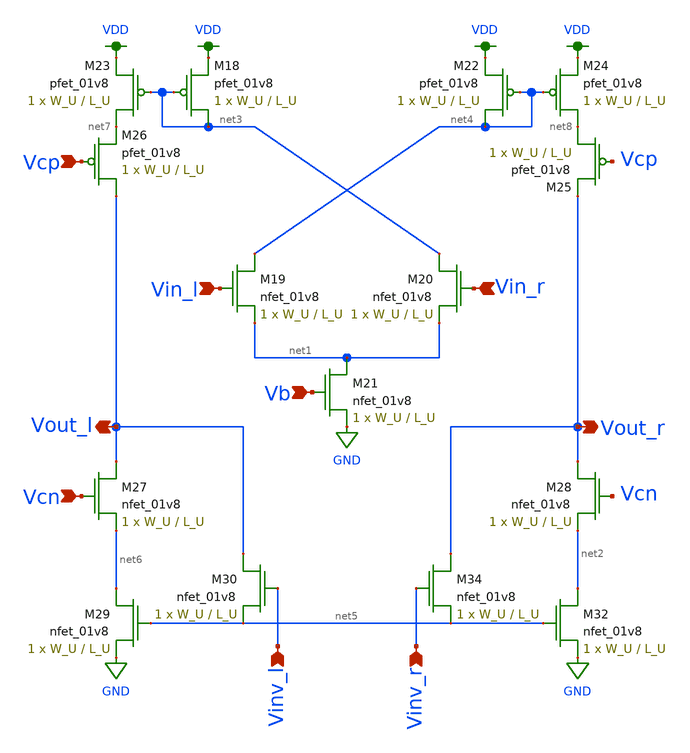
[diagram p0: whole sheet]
** sch_path: schematics/ota.sch
**.subckt ota Vin_l Vin_r Vcp Vb Vinv_l Vinv_r Vcn Vout_r Vout_l
*.ipin Vin_l
*.ipin Vin_r
*.ipin Vcp
*.ipin Vb
*.ipin Vinv_l
*.ipin Vinv_r
*.ipin Vcn
*.opin Vout_r
*.opin Vout_l
XM18 net3 net3 VDD VDD sky130_fd_pr__pfet_01v8 L=L_U W=W_U nf=1 ad='int((nf+1)/2) * W/nf * 0.29' as='int((nf+2)/2) * W/nf * 0.29'
+ pd='2*int((nf+1)/2) * (W/nf + 0.29)' ps='2*int((nf+2)/2) * (W/nf + 0.29)' nrd='0.29 / W' nrs='0.29 / W'
+ sa=0 sb=0 sd=0 mult=1 m=1
XM19 net4 Vin_l net1 GND sky130_fd_pr__nfet_01v8 L=L_U W=W_U nf=1 ad='int((nf+1)/2) * W/nf * 0.29' as='int((nf+2)/2) * W/nf * 0.29'
+ pd='2*int((nf+1)/2) * (W/nf + 0.29)' ps='2*int((nf+2)/2) * (W/nf + 0.29)' nrd='0.29 / W' nrs='0.29 / W'
+ sa=0 sb=0 sd=0 mult=1 m=1
XM20 net3 Vin_r net1 GND sky130_fd_pr__nfet_01v8 L=L_U W=W_U nf=1 ad='int((nf+1)/2) * W/nf * 0.29' as='int((nf+2)/2) * W/nf * 0.29'
+ pd='2*int((nf+1)/2) * (W/nf + 0.29)' ps='2*int((nf+2)/2) * (W/nf + 0.29)' nrd='0.29 / W' nrs='0.29 / W'
+ sa=0 sb=0 sd=0 mult=1 m=1
XM21 net1 Vb GND GND sky130_fd_pr__nfet_01v8 L=L_U W=W_U nf=1 ad='int((nf+1)/2) * W/nf * 0.29' as='int((nf+2)/2) * W/nf * 0.29'
+ pd='2*int((nf+1)/2) * (W/nf + 0.29)' ps='2*int((nf+2)/2) * (W/nf + 0.29)' nrd='0.29 / W' nrs='0.29 / W'
+ sa=0 sb=0 sd=0 mult=1 m=1
XM22 net4 net4 VDD VDD sky130_fd_pr__pfet_01v8 L=L_U W=W_U nf=1 ad='int((nf+1)/2) * W/nf * 0.29' as='int((nf+2)/2) * W/nf * 0.29'
+ pd='2*int((nf+1)/2) * (W/nf + 0.29)' ps='2*int((nf+2)/2) * (W/nf + 0.29)' nrd='0.29 / W' nrs='0.29 / W'
+ sa=0 sb=0 sd=0 mult=1 m=1
XM23 net7 net3 VDD VDD sky130_fd_pr__pfet_01v8 L=L_U W=W_U nf=1 ad='int((nf+1)/2) * W/nf * 0.29' as='int((nf+2)/2) * W/nf * 0.29'
+ pd='2*int((nf+1)/2) * (W/nf + 0.29)' ps='2*int((nf+2)/2) * (W/nf + 0.29)' nrd='0.29 / W' nrs='0.29 / W'
+ sa=0 sb=0 sd=0 mult=1 m=1
XM24 net8 net4 VDD VDD sky130_fd_pr__pfet_01v8 L=L_U W=W_U nf=1 ad='int((nf+1)/2) * W/nf * 0.29' as='int((nf+2)/2) * W/nf * 0.29'
+ pd='2*int((nf+1)/2) * (W/nf + 0.29)' ps='2*int((nf+2)/2) * (W/nf + 0.29)' nrd='0.29 / W' nrs='0.29 / W'
+ sa=0 sb=0 sd=0 mult=1 m=1
XM25 net8 Vcp Vout_r VDD sky130_fd_pr__pfet_01v8 L=L_U W=W_U nf=1 ad='int((nf+1)/2) * W/nf * 0.29' as='int((nf+2)/2) * W/nf * 0.29'
+ pd='2*int((nf+1)/2) * (W/nf + 0.29)' ps='2*int((nf+2)/2) * (W/nf + 0.29)' nrd='0.29 / W' nrs='0.29 / W'
+ sa=0 sb=0 sd=0 mult=1 m=1
XM26 Vout_l Vcp net7 VDD sky130_fd_pr__pfet_01v8 L=L_U W=W_U nf=1 ad='int((nf+1)/2) * W/nf * 0.29' as='int((nf+2)/2) * W/nf * 0.29'
+ pd='2*int((nf+1)/2) * (W/nf + 0.29)' ps='2*int((nf+2)/2) * (W/nf + 0.29)' nrd='0.29 / W' nrs='0.29 / W'
+ sa=0 sb=0 sd=0 mult=1 m=1
XM27 Vout_l Vcn net6 GND sky130_fd_pr__nfet_01v8 L=L_U W=W_U nf=1 ad='int((nf+1)/2) * W/nf * 0.29' as='int((nf+2)/2) * W/nf * 0.29'
+ pd='2*int((nf+1)/2) * (W/nf + 0.29)' ps='2*int((nf+2)/2) * (W/nf + 0.29)' nrd='0.29 / W' nrs='0.29 / W'
+ sa=0 sb=0 sd=0 mult=1 m=1
XM28 Vout_r Vcn net2 GND sky130_fd_pr__nfet_01v8 L=L_U W=W_U nf=1 ad='int((nf+1)/2) * W/nf * 0.29' as='int((nf+2)/2) * W/nf * 0.29'
+ pd='2*int((nf+1)/2) * (W/nf + 0.29)' ps='2*int((nf+2)/2) * (W/nf + 0.29)' nrd='0.29 / W' nrs='0.29 / W'
+ sa=0 sb=0 sd=0 mult=1 m=1
XM29 net6 net5 GND GND sky130_fd_pr__nfet_01v8 L=L_U W=W_U nf=1 ad='int((nf+1)/2) * W/nf * 0.29' as='int((nf+2)/2) * W/nf * 0.29'
+ pd='2*int((nf+1)/2) * (W/nf + 0.29)' ps='2*int((nf+2)/2) * (W/nf + 0.29)' nrd='0.29 / W' nrs='0.29 / W'
+ sa=0 sb=0 sd=0 mult=1 m=1
XM30 Vout_l Vinv_l net5 GND sky130_fd_pr__nfet_01v8 L=L_U W=W_U nf=1 ad='int((nf+1)/2) * W/nf * 0.29'
+ as='int((nf+2)/2) * W/nf * 0.29' pd='2*int((nf+1)/2) * (W/nf + 0.29)' ps='2*int((nf+2)/2) * (W/nf + 0.29)'
+ nrd='0.29 / W' nrs='0.29 / W' sa=0 sb=0 sd=0 mult=1 m=1
XM32 net2 net5 GND GND sky130_fd_pr__nfet_01v8 L=L_U W=W_U nf=1 ad='int((nf+1)/2) * W/nf * 0.29' as='int((nf+2)/2) * W/nf * 0.29'
+ pd='2*int((nf+1)/2) * (W/nf + 0.29)' ps='2*int((nf+2)/2) * (W/nf + 0.29)' nrd='0.29 / W' nrs='0.29 / W'
+ sa=0 sb=0 sd=0 mult=1 m=1
XM34 Vout_r Vinv_r net5 GND sky130_fd_pr__nfet_01v8 L=L_U W=W_U nf=1 ad='int((nf+1)/2) * W/nf * 0.29'
+ as='int((nf+2)/2) * W/nf * 0.29' pd='2*int((nf+1)/2) * (W/nf + 0.29)' ps='2*int((nf+2)/2) * (W/nf + 0.29)'
+ nrd='0.29 / W' nrs='0.29 / W' sa=0 sb=0 sd=0 mult=1 m=1
**.ends
.GLOBAL VDD
.GLOBAL GND
.end
